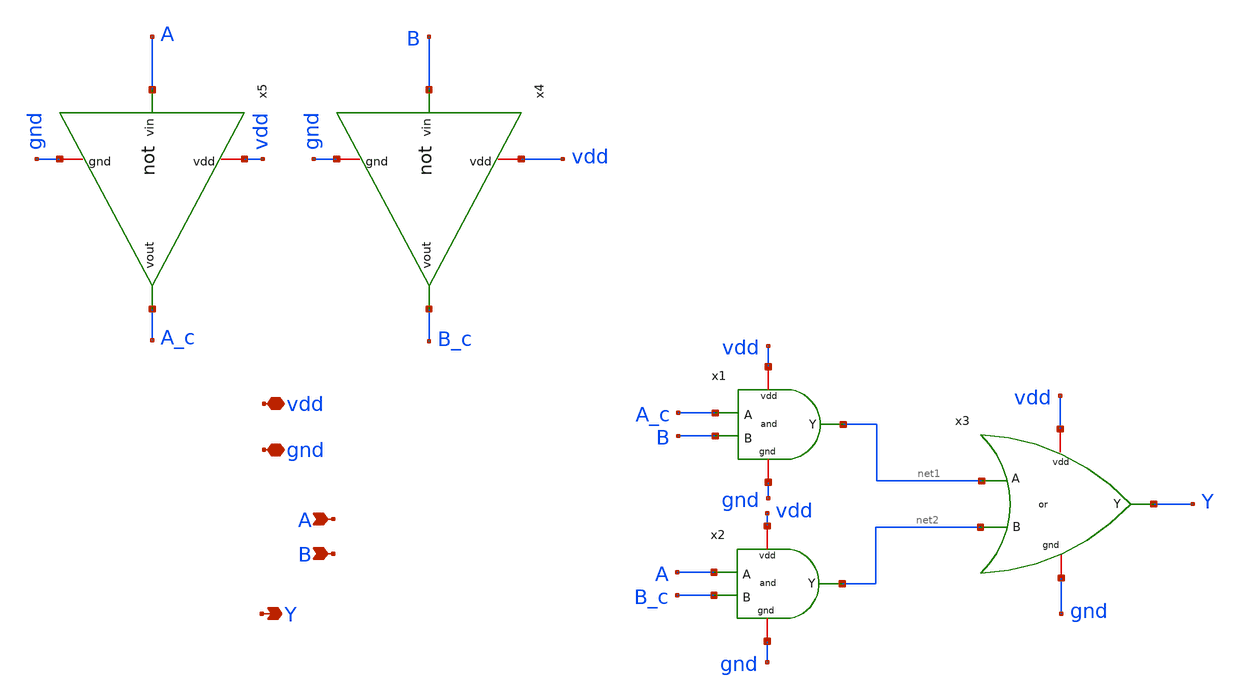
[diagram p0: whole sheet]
** sch_path: LogicGates/xor.sch
**.subckt xor A B vdd gnd Y
*.ipin A
*.ipin B
*.iopin vdd
*.iopin gnd
*.opin Y
x1 vdd gnd A_c B net1 and
x2 vdd gnd A B_c net2 and
x3 vdd gnd net1 net2 Y or
x4 vdd gnd B B_c not
x5 vdd gnd A A_c not
**.ends

* expanding   symbol:  LogicGates/and.sym # of pins=5
** sym_path: LogicGates/and.sym
** sch_path: LogicGates/and.sch
.subckt and vdd gnd A B Y
*.ipin A
*.ipin B
*.iopin vdd
*.iopin gnd
*.opin Y
XM1 net1 A net2 gnd sky130_fd_pr__nfet_01v8 L=0.15 W=1 nf=1 ad='int((nf+1)/2) * W/nf * 0.29' as='int((nf+2)/2) * W/nf * 0.29'
+ pd='2*int((nf+1)/2) * (W/nf + 0.29)' ps='2*int((nf+2)/2) * (W/nf + 0.29)' nrd='0.29 / W' nrs='0.29 / W'
+ sa=0 sb=0 sd=0 mult=1 m=1
XM2 net2 B gnd gnd sky130_fd_pr__nfet_01v8 L=0.15 W=1 nf=1 ad='int((nf+1)/2) * W/nf * 0.29' as='int((nf+2)/2) * W/nf * 0.29'
+ pd='2*int((nf+1)/2) * (W/nf + 0.29)' ps='2*int((nf+2)/2) * (W/nf + 0.29)' nrd='0.29 / W' nrs='0.29 / W'
+ sa=0 sb=0 sd=0 mult=1 m=1
XM3 net1 A vdd vdd sky130_fd_pr__pfet_01v8 L=0.15 W=2 nf=1 ad='int((nf+1)/2) * W/nf * 0.29' as='int((nf+2)/2) * W/nf * 0.29'
+ pd='2*int((nf+1)/2) * (W/nf + 0.29)' ps='2*int((nf+2)/2) * (W/nf + 0.29)' nrd='0.29 / W' nrs='0.29 / W'
+ sa=0 sb=0 sd=0 mult=1 m=1
XM4 net1 B vdd vdd sky130_fd_pr__pfet_01v8 L=0.15 W=2 nf=1 ad='int((nf+1)/2) * W/nf * 0.29' as='int((nf+2)/2) * W/nf * 0.29'
+ pd='2*int((nf+1)/2) * (W/nf + 0.29)' ps='2*int((nf+2)/2) * (W/nf + 0.29)' nrd='0.29 / W' nrs='0.29 / W'
+ sa=0 sb=0 sd=0 mult=1 m=1
x1 vdd gnd net1 Y not
.ends


* expanding   symbol:  LogicGates/or.sym # of pins=5
** sym_path: LogicGates/or.sym
** sch_path: LogicGates/or.sch
.subckt or vdd gnd A B Y
*.ipin A
*.ipin B
*.iopin vdd
*.iopin gnd
*.opin Y
XM1 net1 A gnd gnd sky130_fd_pr__nfet_01v8 L=0.15 W=1 nf=1 ad='int((nf+1)/2) * W/nf * 0.29' as='int((nf+2)/2) * W/nf * 0.29'
+ pd='2*int((nf+1)/2) * (W/nf + 0.29)' ps='2*int((nf+2)/2) * (W/nf + 0.29)' nrd='0.29 / W' nrs='0.29 / W'
+ sa=0 sb=0 sd=0 mult=1 m=1
XM2 net1 B gnd gnd sky130_fd_pr__nfet_01v8 L=0.15 W=1 nf=1 ad='int((nf+1)/2) * W/nf * 0.29' as='int((nf+2)/2) * W/nf * 0.29'
+ pd='2*int((nf+1)/2) * (W/nf + 0.29)' ps='2*int((nf+2)/2) * (W/nf + 0.29)' nrd='0.29 / W' nrs='0.29 / W'
+ sa=0 sb=0 sd=0 mult=1 m=1
XM3 net2 A vdd vdd sky130_fd_pr__pfet_01v8 L=0.15 W=2 nf=1 ad='int((nf+1)/2) * W/nf * 0.29' as='int((nf+2)/2) * W/nf * 0.29'
+ pd='2*int((nf+1)/2) * (W/nf + 0.29)' ps='2*int((nf+2)/2) * (W/nf + 0.29)' nrd='0.29 / W' nrs='0.29 / W'
+ sa=0 sb=0 sd=0 mult=1 m=1
XM4 net1 B net2 vdd sky130_fd_pr__pfet_01v8 L=0.15 W=2 nf=1 ad='int((nf+1)/2) * W/nf * 0.29' as='int((nf+2)/2) * W/nf * 0.29'
+ pd='2*int((nf+1)/2) * (W/nf + 0.29)' ps='2*int((nf+2)/2) * (W/nf + 0.29)' nrd='0.29 / W' nrs='0.29 / W'
+ sa=0 sb=0 sd=0 mult=1 m=1
x1 vdd gnd net1 Y not
.ends


* expanding   symbol:  LogicGates/not.sym # of pins=4
** sym_path: LogicGates/not.sym
** sch_path: LogicGates/not.sch
.subckt not vdd gnd vin vout
*.ipin vin
*.iopin vdd
*.iopin gnd
*.opin vout
XM2 vout vin vdd vdd sky130_fd_pr__pfet_01v8 L=0.15 W=2 nf=1 ad='int((nf+1)/2) * W/nf * 0.29' as='int((nf+2)/2) * W/nf * 0.29'
+ pd='2*int((nf+1)/2) * (W/nf + 0.29)' ps='2*int((nf+2)/2) * (W/nf + 0.29)' nrd='0.29 / W' nrs='0.29 / W'
+ sa=0 sb=0 sd=0 mult=1 m=1
XM1 vout vin gnd gnd sky130_fd_pr__nfet_01v8 L=0.15 W=1 nf=1 ad='int((nf+1)/2) * W/nf * 0.29' as='int((nf+2)/2) * W/nf * 0.29'
+ pd='2*int((nf+1)/2) * (W/nf + 0.29)' ps='2*int((nf+2)/2) * (W/nf + 0.29)' nrd='0.29 / W' nrs='0.29 / W'
+ sa=0 sb=0 sd=0 mult=1 m=1
.ends

.end
